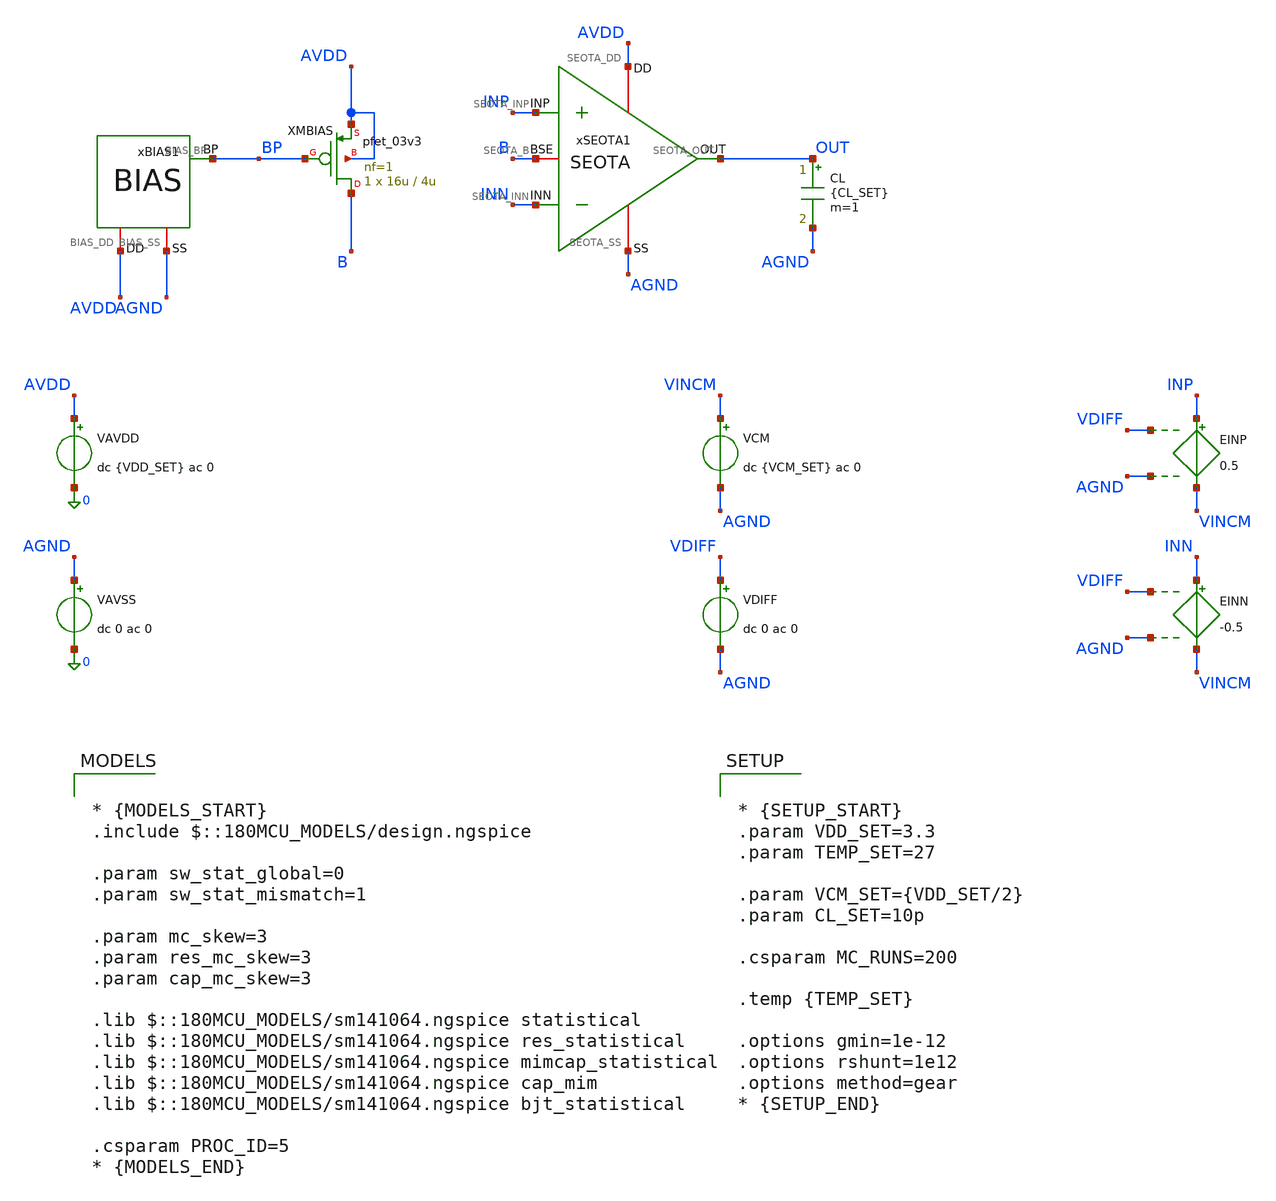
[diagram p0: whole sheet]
** sch_path: Design_Files/IC Design/Testbench/ANALOG_BLOCKS/SEOTA/Open_Loop/SEOTA_TB_OL_MC.sch
**.subckt SEOTA_TB_OL_MC
VAVDD AVDD 0 dc {VDD_SET} ac 0
.save i(vavdd)
CL OUT AGND {CL_SET} m=1
VCM VINCM AGND dc {VCM_SET} ac 0
VDIFF VDIFF AGND dc 0 ac 0
xSEOTA1 AVDD AGND INP INN OUT B SEOTA
VAVSS AGND 0 dc 0 ac 0
EINN INN VINCM VDIFF AGND -0.5
EINP INP VINCM VDIFF AGND 0.5
xBIAS1 AVDD AGND BP BIAS
XMBIAS B BP AVDD AVDD pfet_03v3 L=4u W=16u nf=1 ad='int((nf+1)/2) * W/nf * 0.18u' as='int((nf+2)/2) * W/nf * 0.18u'
+ pd='2*int((nf+1)/2) * (W/nf + 0.18u)' ps='2*int((nf+2)/2) * (W/nf + 0.18u)' nrd='0.18u / W' nrs='0.18u / W'
+ sa=0 sb=0 sd=0 m=1
**** begin user architecture code

* {MODELS_START}
.include $::180MCU_MODELS/design.ngspice

.param sw_stat_global=0
.param sw_stat_mismatch=1

.param mc_skew=3
.param res_mc_skew=3
.param cap_mc_skew=3

.lib $::180MCU_MODELS/sm141064.ngspice statistical
.lib $::180MCU_MODELS/sm141064.ngspice res_statistical
.lib $::180MCU_MODELS/sm141064.ngspice mimcap_statistical
.lib $::180MCU_MODELS/sm141064.ngspice cap_mim
.lib $::180MCU_MODELS/sm141064.ngspice bjt_statistical

.csparam PROC_ID=5
* {MODELS_END}



* {SETUP_START}
.param VDD_SET=3.3
.param TEMP_SET=27

.param VCM_SET={VDD_SET/2}
.param CL_SET=10p

.csparam MC_RUNS=200

.temp {TEMP_SET}

.options gmin=1e-12
.options rshunt=1e12
.options method=gear
* {SETUP_END}




* {MEAS_START}

.control

destroy all

set noaskquit
set wr_singlescale
unset wr_vecnames

option klu
option numdgt=15
option method=gear
option maxord=2
option plotwinsize=0


let mode_index=0
dowhile mode_index < 3
if mode_index = 0
set proc=MM
alterparam sw_stat_global=0
alterparam sw_stat_mismatch=1
end
if mode_index = 1
set proc=GL
alterparam sw_stat_global=1
alterparam sw_stat_mismatch=0
end
if mode_index = 2
set proc=FULL
alterparam sw_stat_global=1
alterparam sw_stat_mismatch=1
end
reset

shell mkdir -p /foss/designs/ECG_Acquisition_IC/Measurement_Results/IC_Simulation/ANALOG_BLOCKS/SEOTA/{$proc}.Result_txt

shell rm -f /foss/designs/ECG_Acquisition_IC/Measurement_Results/IC_Simulation/ANALOG_BLOCKS/SEOTA/{$proc}.Result_txt/{$proc}.ol_mc_summary.txt
shell rm -f /foss/designs/ECG_Acquisition_IC/Measurement_Results/IC_Simulation/ANALOG_BLOCKS/SEOTA/{$proc}.Result_txt/{$proc}.ol_mc_debug_op.txt


echo run vos_V center_error_V ol_gain_1Hz ol_gain_dB ugf_Hz phase_ugf_deg pm_deg vout_center_V b_V ibias_A
+ idd_A power_W > /foss/designs/ECG_Acquisition_IC/Measurement_Results/IC_Simulation/ANALOG_BLOCKS/SEOTA/{$proc}.Result_txt/{$proc}.ol_mc_summary.txt

echo run vos_V vout_zero_V vout_center_V center_error_V net1_V net2_V net3_V net4_V b_V ibias_A idd_A
+ power_W > /foss/designs/ECG_Acquisition_IC/Measurement_Results/IC_Simulation/ANALOG_BLOCKS/SEOTA/{$proc}.Result_txt/{$proc}.ol_mc_debug_op.txt


let run=1
let mc_runs=$&MC_RUNS


dowhile run <= mc_runs


set runnum=$&run

setseed $runnum
mc_source


option klu
option numdgt=15
option method=gear
option maxord=2
option plotwinsize=0


* DEFAULT VALUES

set vos_val=0
set vout_zero_val=0
set vout_center_val=0
set center_error_val=0

set gain_val=0
set gain_db_val=0
set ugf_val=0
set phase_val=0
set pm_val=0

set net1_val=0
set net2_val=0
set net3_val=0
set net4_val=0

set b_val=0
set ibias_val=0
set idd_val=0
set power_val=0


* INITIAL SOURCES

alter @VCM[DC]=1.65
alter @VDIFF[DC]=0

alter @VCM[ACMAG]=0
alter @VDIFF[ACMAG]=0
alter @VAVDD[ACMAG]=0
alter @VAVSS[ACMAG]=0


save all
save @m.xmbias.m0[id]


* ZERO-DIFFERENTIAL OP

op

let vout_zero=v(OUT)-v(AGND)

set vout_zero_val=$&vout_zero


destroy all


* FIND OFFSET

alter @VDIFF[DC]=0

dc VDIFF -50m 50m 10u

meas dc vos_center when v(OUT)=1.65 cross=1

set vos_val=$&vos_center


destroy all


* CENTER OTA

alter @VDIFF[DC]=$vos_val

alter @VCM[ACMAG]=0
alter @VDIFF[ACMAG]=0
alter @VAVDD[ACMAG]=0
alter @VAVSS[ACMAG]=0


save all
save @m.xmbias.m0[id]


op


let vout_center=v(OUT)-v(AGND)
let center_error=vout_center-1.65

let b_op=v(B)-v(AGND)

let net1_op=v(xseota1.net1)-v(AGND)
let net2_op=v(xseota1.net2)-v(AGND)
let net3_op=v(xseota1.net3)-v(AGND)
let net4_op=v(xseota1.net4)-v(AGND)

let ibias=abs(@m.xmbias.m0[id])
let idd_total=abs(vavdd#branch)
let power_total=(v(AVDD)-v(AGND))*idd_total


set vout_center_val=$&vout_center
set center_error_val=$&center_error

set b_val=$&b_op

set net1_val=$&net1_op
set net2_val=$&net2_op
set net3_val=$&net3_op
set net4_val=$&net4_op

set ibias_val=$&ibias
set idd_val=$&idd_total
set power_val=$&power_total


echo $runnum $vos_val $vout_zero_val $vout_center_val $center_error_val $net1_val $net2_val $net3_val
+ $net4_val $b_val $ibias_val $idd_val $power_val >> /foss/designs/ECG_Acquisition_IC/Measurement_Results/IC_Simulation/ANALOG_BLOCKS/SEOTA/{$proc}.Result_txt/{$proc}.ol_mc_debug_op.txt


destroy all


* OPEN-LOOP AC AT CENTERED OP

alter @VDIFF[DC]=$vos_val

alter @VCM[ACMAG]=0
alter @VDIFF[ACMAG]=1
alter @VDIFF[ACPHASE]=0
alter @VAVDD[ACMAG]=0
alter @VAVSS[ACMAG]=0


ac dec 200 0.01 1G


let vin_diff=v(INP)-v(INN)
let vout_ac=v(OUT)-v(AGND)

let ol_tf=vout_ac/vin_diff

let ol_gain=mag(ol_tf)
let ol_gain_db=db(ol_tf)
let ol_phase=(180/3.141592653589793)*cph(ol_tf)


meas ac ol_gain_1 find ol_gain at=1
meas ac ol_gain_db_1 find ol_gain_db at=1

set gain_val=$&ol_gain_1
set gain_db_val=$&ol_gain_db_1


meas ac ugf_meas when ol_gain=1 cross=1

set ugf_val=$&ugf_meas


meas ac phase_ugf find ol_phase at=$ugf_val

set phase_val=$&phase_ugf


let pm_calc=180+phase_ugf

set pm_val=$&pm_calc


echo $runnum $vos_val $center_error_val $gain_val $gain_db_val $ugf_val $phase_val $pm_val $vout_center_val
+ $b_val $ibias_val $idd_val $power_val >> /foss/designs/ECG_Acquisition_IC/Measurement_Results/IC_Simulation/ANALOG_BLOCKS/SEOTA/{$proc}.Result_txt/{$proc}.ol_mc_summary.txt


destroy all

let run=run+1


end


let mode_index=mode_index+1
end

quit

.endc
* {MEAS_END}


**** end user architecture code
**.ends
.end
